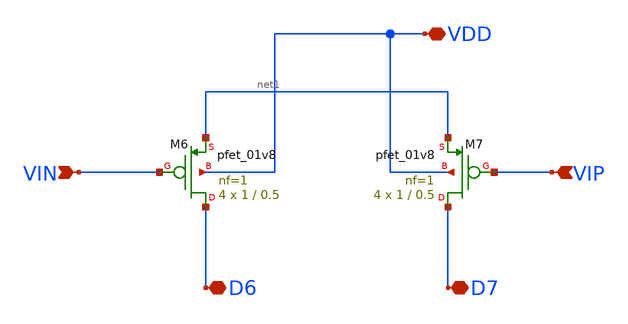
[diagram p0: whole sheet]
** sch_path: opamp/xschem/untitled-1.sch
**.subckt untitled-1 VIP VIN VDD D6 D7
*.ipin VIP
*.ipin VIN
*.iopin VDD
*.iopin D6
*.iopin D7
XM6 D6 VIN net1 VDD sky130_fd_pr__pfet_01v8 L=0.5 W=1 nf=1 ad='int((nf+1)/2) * W/nf * 0.29' as='int((nf+2)/2) * W/nf * 0.29'
+ pd='2*int((nf+1)/2) * (W/nf + 0.29)' ps='2*int((nf+2)/2) * (W/nf + 0.29)' nrd='0.29 / W' nrs='0.29 / W'
+ sa=0 sb=0 sd=0 mult=4 m=4
XM7 D7 VIP net1 VDD sky130_fd_pr__pfet_01v8 L=0.5 W=1 nf=1 ad='int((nf+1)/2) * W/nf * 0.29' as='int((nf+2)/2) * W/nf * 0.29'
+ pd='2*int((nf+1)/2) * (W/nf + 0.29)' ps='2*int((nf+2)/2) * (W/nf + 0.29)' nrd='0.29 / W' nrs='0.29 / W'
+ sa=0 sb=0 sd=0 mult=4 m=4
**.ends
.end
